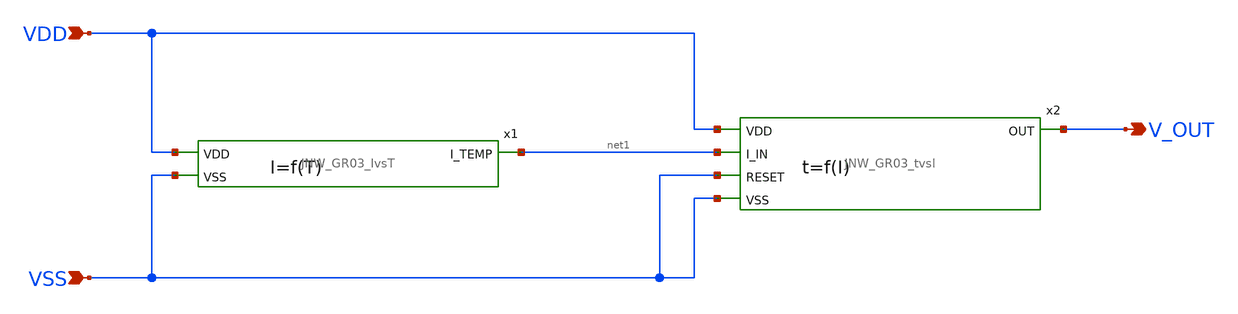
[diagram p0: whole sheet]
** sch_path: design/JNW_GR03_SKY130A/JNW_GR03_General.sch
**.subckt JNW_GR03_General VDD VSS V_OUT
*.ipin VDD
*.ipin VSS
*.opin V_OUT
x1 VDD net1 VSS JNW_GR03_IvsT
x2 VDD net1 V_OUT VSS VSS JNW_GR03_tvsI
**.ends
.end
